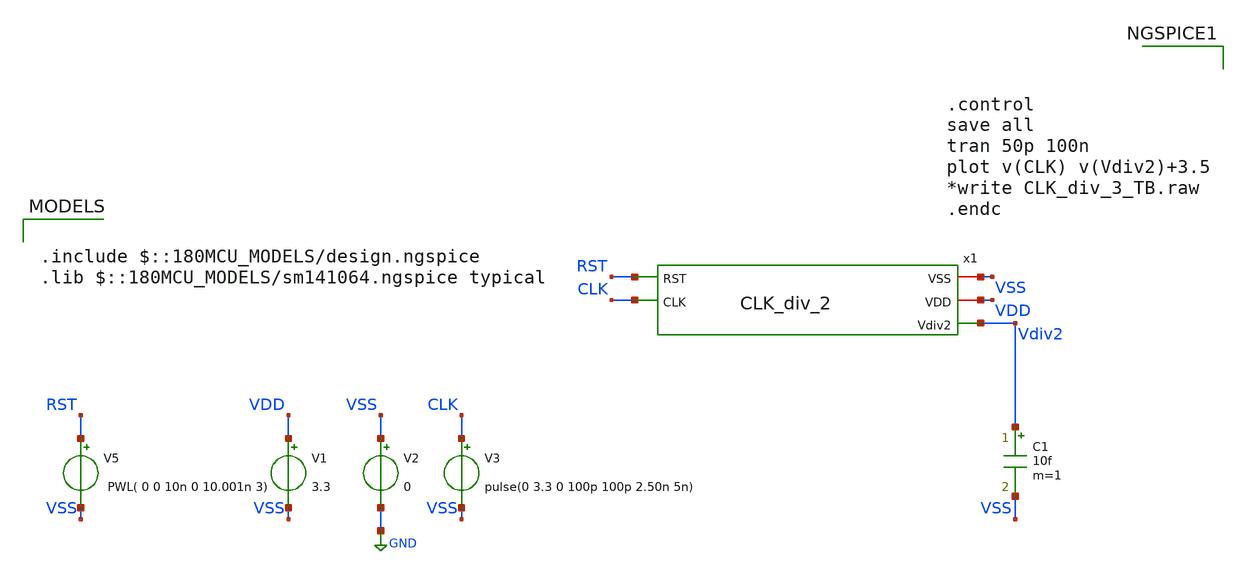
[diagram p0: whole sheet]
** sch_path: Clock_Generator_PAKISTAN_02/Schematics/CLK_div_2_TB.sch
**.subckt CLK_div_2_TB
V1 VDD VSS 3.3
V2 VSS GND 0
V3 CLK VSS pulse(0 3.3 0 100p 100p 2.50n 5n)
C1 Vdiv2 VSS 10f m=1
V5 RST VSS PWL( 0 0 10n 0 10.001n 3)
x1 VSS VDD Vdiv2 RST CLK CLK_div_2
**** begin user architecture code

.include $::180MCU_MODELS/design.ngspice
.lib $::180MCU_MODELS/sm141064.ngspice typical




.control
save all
tran 50p 100n
plot v(CLK) v(Vdiv2)+3.5
*write CLK_div_3_TB.raw
.endc


**** end user architecture code
**.ends
.GLOBAL GND
.end
